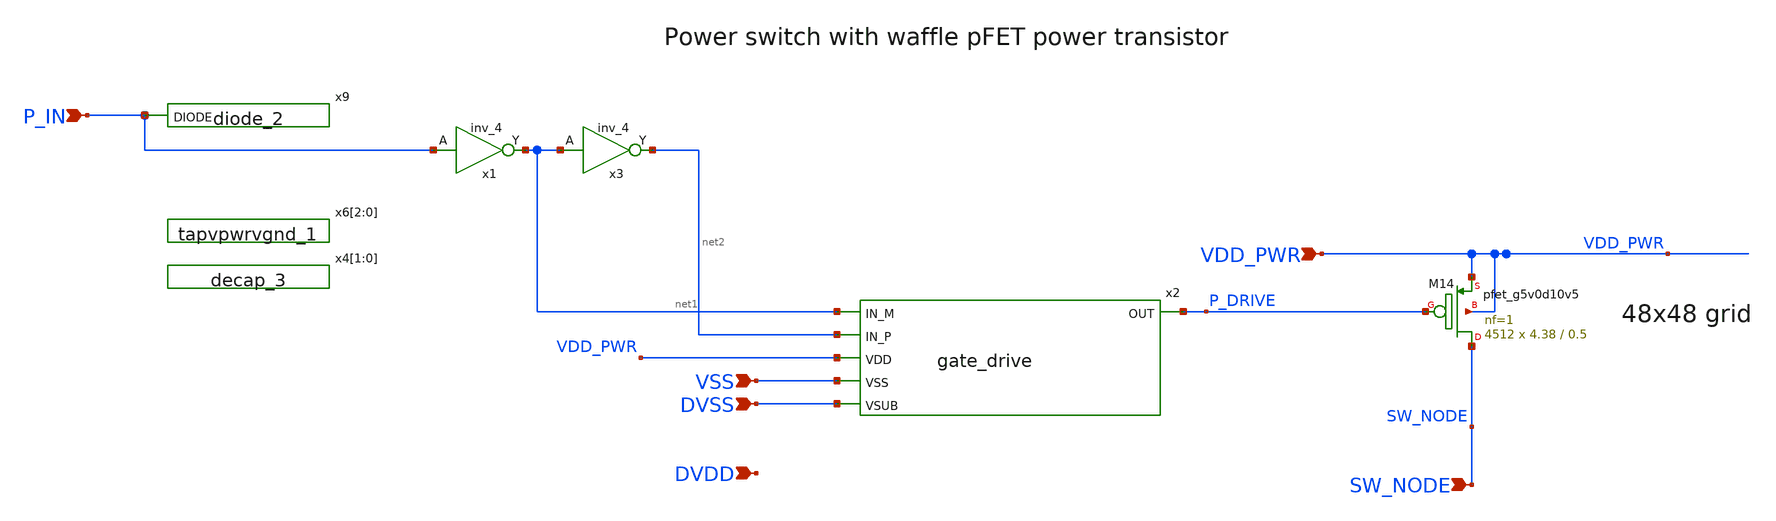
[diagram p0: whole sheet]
** sch_path: xschem/power_stage.sch
**.subckt power_stage P_IN SW_NODE VDD_PWR VSS DVSS DVDD
*.ipin P_IN
*.ipin SW_NODE
*.ipin VDD_PWR
*.ipin VSS
*.ipin DVSS
*.ipin DVDD
XM14 SW_NODE P_DRIVE VDD_PWR VDD_PWR sky130_fd_pr__pfet_g5v0d10v5 L=0.5 W=4.38 nf=1 ad='int((nf+1)/2) * W/nf * 0.29'
+ as='int((nf+2)/2) * W/nf * 0.29' pd='2*int((nf+1)/2) * (W/nf + 0.29)' ps='2*int((nf+2)/2) * (W/nf + 0.29)'
+ nrd='0.29 / W' nrs='0.29 / W' sa=0 sb=0 sd=0 mult=4512 m=4512
x2 net1 net2 P_DRIVE VDD_PWR VSS DVSS gate_drive
x1 P_IN DVSS DVSS DVDD DVDD net1 sky130_fd_sc_hd__inv_4
x3 net1 DVSS DVSS DVDD DVDD net2 sky130_fd_sc_hd__inv_4
x4[1] DVSS DVSS DVDD DVDD sky130_fd_sc_hd__decap_3
x4[0] DVSS DVSS DVDD DVDD sky130_fd_sc_hd__decap_3
x6[2] DVSS DVDD sky130_fd_sc_hd__tapvpwrvgnd_1
x6[1] DVSS DVDD sky130_fd_sc_hd__tapvpwrvgnd_1
x6[0] DVSS DVDD sky130_fd_sc_hd__tapvpwrvgnd_1
x9 P_IN DVSS DVSS DVDD DVDD sky130_fd_sc_hd__diode_2
**.ends

* expanding   symbol:  gate_drive.sym # of pins=6
** sym_path: xschem/gate_drive.sym
** sch_path: xschem/gate_drive.sch
.subckt gate_drive IN_M IN_P OUT VDD VSS VSUB
*.ipin IN_M
*.ipin IN_P
*.ipin VDD
*.ipin VSS
*.opin OUT
*.ipin VSUB
XM1 net1 IN_P VSS VSS sky130_fd_pr__nfet_g5v0d10v5 L=0.5 W=2 nf=1 ad='int((nf+1)/2) * W/nf * 0.29' as='int((nf+2)/2) * W/nf * 0.29'
+ pd='2*int((nf+1)/2) * (W/nf + 0.29)' ps='2*int((nf+2)/2) * (W/nf + 0.29)' nrd='0.29 / W' nrs='0.29 / W'
+ sa=0 sb=0 sd=0 mult=2 m=2
XM2 net1 S1_N VDD VDD sky130_fd_pr__pfet_g5v0d10v5 L=0.5 W=4 nf=1 ad='int((nf+1)/2) * W/nf * 0.29' as='int((nf+2)/2) * W/nf * 0.29'
+ pd='2*int((nf+1)/2) * (W/nf + 0.29)' ps='2*int((nf+2)/2) * (W/nf + 0.29)' nrd='0.29 / W' nrs='0.29 / W'
+ sa=0 sb=0 sd=0 mult=2 m=2
XM3 S1_N IN_M VSS VSS sky130_fd_pr__nfet_g5v0d10v5 L=0.5 W=2 nf=1 ad='int((nf+1)/2) * W/nf * 0.29' as='int((nf+2)/2) * W/nf * 0.29'
+ pd='2*int((nf+1)/2) * (W/nf + 0.29)' ps='2*int((nf+2)/2) * (W/nf + 0.29)' nrd='0.29 / W' nrs='0.29 / W'
+ sa=0 sb=0 sd=0 mult=2 m=2
XM4 S1_N net1 VDD VDD sky130_fd_pr__pfet_g5v0d10v5 L=0.5 W=4 nf=1 ad='int((nf+1)/2) * W/nf * 0.29' as='int((nf+2)/2) * W/nf * 0.29'
+ pd='2*int((nf+1)/2) * (W/nf + 0.29)' ps='2*int((nf+2)/2) * (W/nf + 0.29)' nrd='0.29 / W' nrs='0.29 / W'
+ sa=0 sb=0 sd=0 mult=2 m=2
XM5 S2_N S1_N VDD VDD sky130_fd_pr__pfet_g5v0d10v5 L=0.5 W=15 nf=1 ad='int((nf+1)/2) * W/nf * 0.29' as='int((nf+2)/2) * W/nf * 0.29'
+ pd='2*int((nf+1)/2) * (W/nf + 0.29)' ps='2*int((nf+2)/2) * (W/nf + 0.29)' nrd='0.29 / W' nrs='0.29 / W'
+ sa=0 sb=0 sd=0 mult=2 m=2
XM6 S2_N S1_N VSS VSS sky130_fd_pr__nfet_g5v0d10v5 L=0.5 W=7 nf=1 ad='int((nf+1)/2) * W/nf * 0.29' as='int((nf+2)/2) * W/nf * 0.29'
+ pd='2*int((nf+1)/2) * (W/nf + 0.29)' ps='2*int((nf+2)/2) * (W/nf + 0.29)' nrd='0.29 / W' nrs='0.29 / W'
+ sa=0 sb=0 sd=0 mult=2 m=2
XM7 S3_N S2_N VDD VDD sky130_fd_pr__pfet_g5v0d10v5 L=0.5 W=15 nf=1 ad='int((nf+1)/2) * W/nf * 0.29' as='int((nf+2)/2) * W/nf * 0.29'
+ pd='2*int((nf+1)/2) * (W/nf + 0.29)' ps='2*int((nf+2)/2) * (W/nf + 0.29)' nrd='0.29 / W' nrs='0.29 / W'
+ sa=0 sb=0 sd=0 mult=6 m=6
XM8 S3_N S2_N VSS VSS sky130_fd_pr__nfet_g5v0d10v5 L=0.5 W=7 nf=1 ad='int((nf+1)/2) * W/nf * 0.29' as='int((nf+2)/2) * W/nf * 0.29'
+ pd='2*int((nf+1)/2) * (W/nf + 0.29)' ps='2*int((nf+2)/2) * (W/nf + 0.29)' nrd='0.29 / W' nrs='0.29 / W'
+ sa=0 sb=0 sd=0 mult=6 m=6
XM9 S4_N S3_N VDD VDD sky130_fd_pr__pfet_g5v0d10v5 L=0.5 W=15 nf=1 ad='int((nf+1)/2) * W/nf * 0.29' as='int((nf+2)/2) * W/nf * 0.29'
+ pd='2*int((nf+1)/2) * (W/nf + 0.29)' ps='2*int((nf+2)/2) * (W/nf + 0.29)' nrd='0.29 / W' nrs='0.29 / W'
+ sa=0 sb=0 sd=0 mult=20 m=20
XM10 S4_N S3_N VSS VSS sky130_fd_pr__nfet_g5v0d10v5 L=0.5 W=7 nf=1 ad='int((nf+1)/2) * W/nf * 0.29' as='int((nf+2)/2) * W/nf * 0.29'
+ pd='2*int((nf+1)/2) * (W/nf + 0.29)' ps='2*int((nf+2)/2) * (W/nf + 0.29)' nrd='0.29 / W' nrs='0.29 / W'
+ sa=0 sb=0 sd=0 mult=20 m=20
XM11 OUT S4_N VDD VDD sky130_fd_pr__pfet_g5v0d10v5 L=0.5 W=15 nf=1 ad='int((nf+1)/2) * W/nf * 0.29' as='int((nf+2)/2) * W/nf * 0.29'
+ pd='2*int((nf+1)/2) * (W/nf + 0.29)' ps='2*int((nf+2)/2) * (W/nf + 0.29)' nrd='0.29 / W' nrs='0.29 / W'
+ sa=0 sb=0 sd=0 mult=60 m=60
XM12 OUT S4_N VSS VSS sky130_fd_pr__nfet_g5v0d10v5 L=0.5 W=7 nf=1 ad='int((nf+1)/2) * W/nf * 0.29' as='int((nf+2)/2) * W/nf * 0.29'
+ pd='2*int((nf+1)/2) * (W/nf + 0.29)' ps='2*int((nf+2)/2) * (W/nf + 0.29)' nrd='0.29 / W' nrs='0.29 / W'
+ sa=0 sb=0 sd=0 mult=60 m=60
.ends

.end
